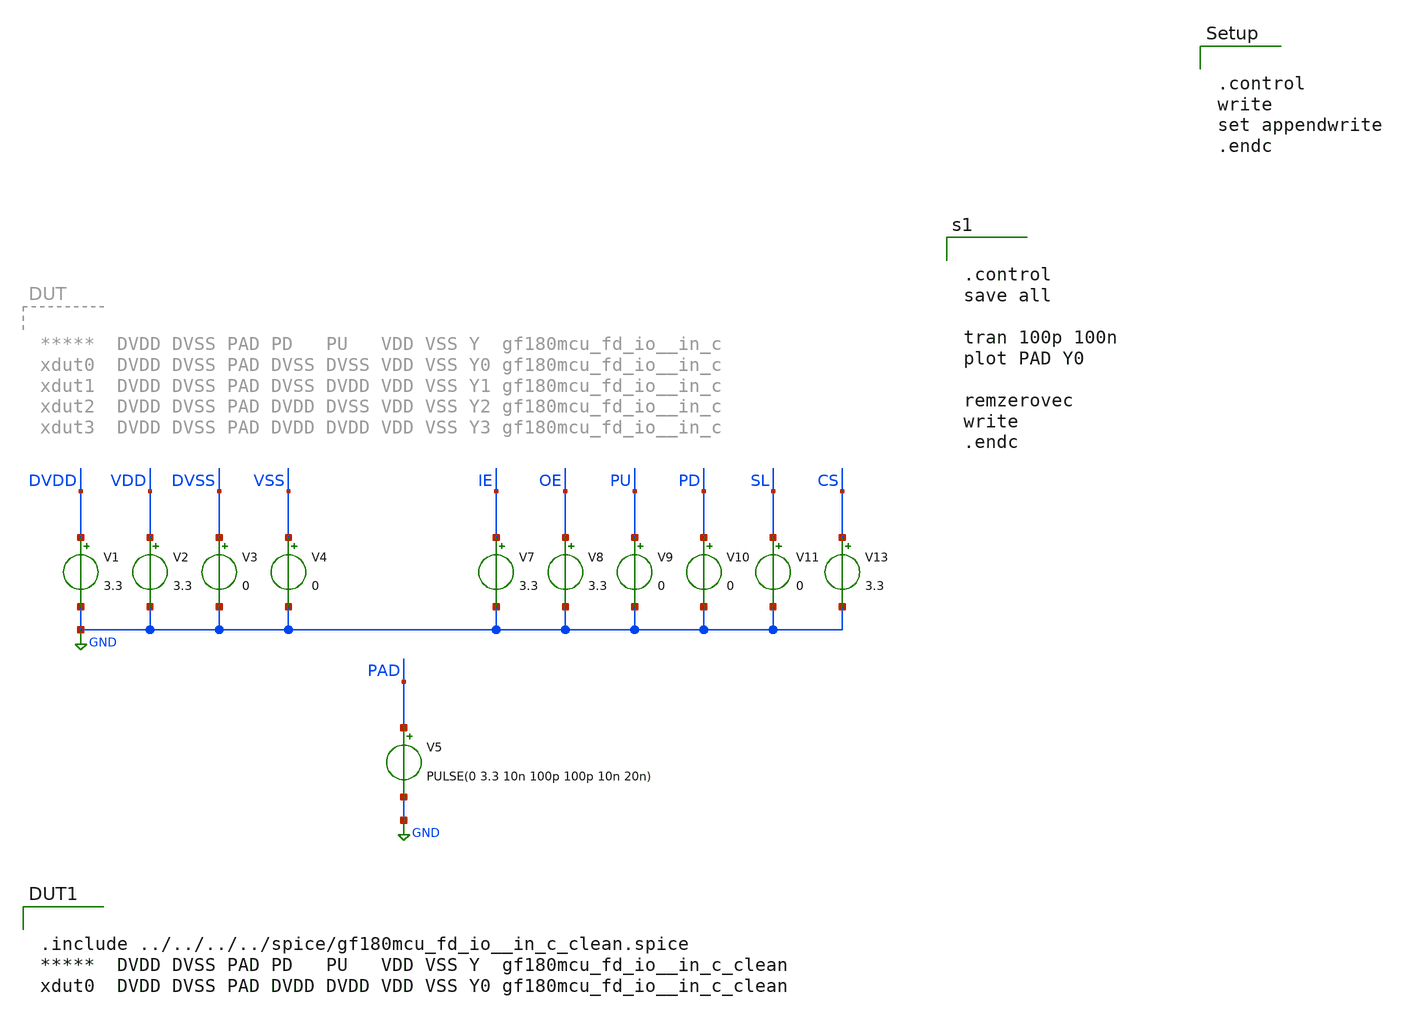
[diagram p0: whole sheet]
** sch_path: padframe/switching_in_c/test/switching_in_c.sch

.include $env(PDK_ROOT)/$env(PDK)/libs.tech/ngspice/design.ngspice
.lib $env(PDK_ROOT)/$env(PDK)/libs.tech/ngspice/sm141064.ngspice typical
.lib $env(PDK_ROOT)/$env(PDK)/libs.tech/ngspice/sm141064.ngspice diode_typical
.lib $env(PDK_ROOT)/$env(PDK)/libs.tech/ngspice/sm141064.ngspice res_typical
.lib $env(PDK_ROOT)/$env(PDK)/libs.tech/ngspice/sm141064.ngspice mimcap_typical
.lib $env(PDK_ROOT)/$env(PDK)/libs.tech/ngspice/sm141064.ngspice moscap_typical
.lib $env(PDK_ROOT)/$env(PDK)/libs.tech/ngspice/sm141064.ngspice bjt_typical

.include $env(PDK_ROOT)/$env(PDK)/libs.ref/gf180mcu_fd_io/spice/gf180mcu_fd_io.spice


.control
write
set appendwrite
.endc
**.subckt switching_in_c
V1 DVDD GND 3.3
V2 VDD GND 3.3
V3 DVSS GND 0
V4 VSS GND 0
V5 PAD GND PULSE(0 3.3 10n 100p 100p 10n 20n)
V7 IE GND 3.3
V8 OE GND 3.3
V9 PU GND 0
V10 PD GND 0
V11 SL GND 0
V13 CS GND 3.3
**** begin user architecture code


.control
save all

tran 100p 100n
plot PAD Y0

remzerovec
write
.endc



.include ../../../../spice/gf180mcu_fd_io__in_c_clean.spice
*****  DVDD DVSS PAD PD   PU   VDD VSS Y  gf180mcu_fd_io__in_c_clean
xdut0  DVDD DVSS PAD DVDD DVDD VDD VSS Y0 gf180mcu_fd_io__in_c_clean

**** end user architecture code
**.ends
.GLOBAL GND
.end
